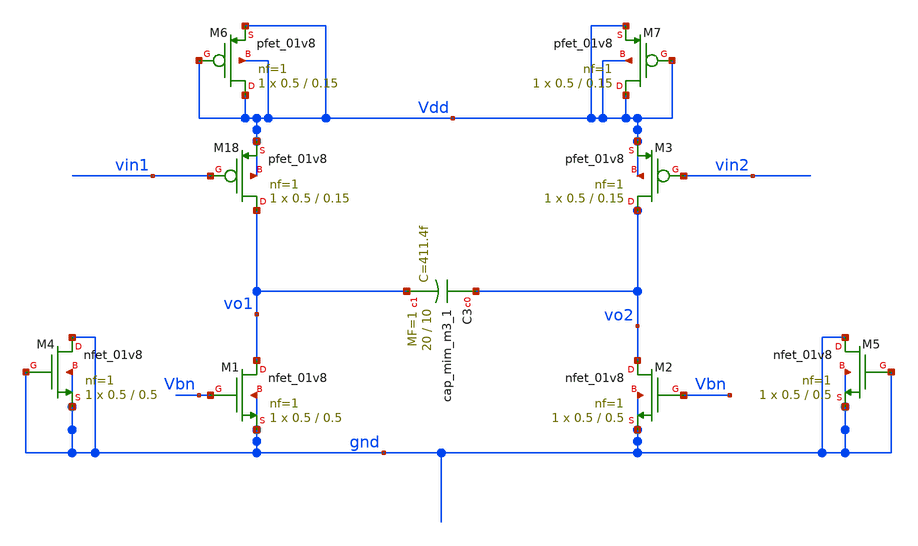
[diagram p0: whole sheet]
** sch_path: xschem/xschemfiles/integrator2.sch
**.subckt integrator2
XM3 vo2 vin2 Vdd Vdd sky130_fd_pr__pfet_01v8 L=0.15 W=0.5 nf=1 ad='int((nf+1)/2) * W/nf * 0.29' as='int((nf+2)/2) * W/nf * 0.29'
+ pd='2*int((nf+1)/2) * (W/nf + 0.29)' ps='2*int((nf+2)/2) * (W/nf + 0.29)' nrd='0.29 / W' nrs='0.29 / W'
+ sa=0 sb=0 sd=0 mult=1 m=1
XM1 vo1 Vbn gnd gnd sky130_fd_pr__nfet_01v8 L=0.5 W=0.5 nf=1 ad='int((nf+1)/2) * W/nf * 0.29' as='int((nf+2)/2) * W/nf * 0.29'
+ pd='2*int((nf+1)/2) * (W/nf + 0.29)' ps='2*int((nf+2)/2) * (W/nf + 0.29)' nrd='0.29 / W' nrs='0.29 / W'
+ sa=0 sb=0 sd=0 mult=1 m=1
XM2 vo2 Vbn gnd gnd sky130_fd_pr__nfet_01v8 L=0.5 W=0.5 nf=1 ad='int((nf+1)/2) * W/nf * 0.29' as='int((nf+2)/2) * W/nf * 0.29'
+ pd='2*int((nf+1)/2) * (W/nf + 0.29)' ps='2*int((nf+2)/2) * (W/nf + 0.29)' nrd='0.29 / W' nrs='0.29 / W'
+ sa=0 sb=0 sd=0 mult=1 m=1
XC3 vo2 vo1 sky130_fd_pr__cap_mim_m3_1 W=20 L=10 MF=1 m=1
XM18 vo1 vin1 Vdd Vdd sky130_fd_pr__pfet_01v8 L=0.15 W=0.5 nf=1 ad='int((nf+1)/2) * W/nf * 0.29' as='int((nf+2)/2) * W/nf * 0.29'
+ pd='2*int((nf+1)/2) * (W/nf + 0.29)' ps='2*int((nf+2)/2) * (W/nf + 0.29)' nrd='0.29 / W' nrs='0.29 / W'
+ sa=0 sb=0 sd=0 mult=1 m=1
XM4 gnd gnd gnd gnd sky130_fd_pr__nfet_01v8 L=0.5 W=0.5 nf=1 ad='int((nf+1)/2) * W/nf * 0.29' as='int((nf+2)/2) * W/nf * 0.29'
+ pd='2*int((nf+1)/2) * (W/nf + 0.29)' ps='2*int((nf+2)/2) * (W/nf + 0.29)' nrd='0.29 / W' nrs='0.29 / W'
+ sa=0 sb=0 sd=0 mult=1 m=1
XM5 gnd gnd gnd gnd sky130_fd_pr__nfet_01v8 L=0.5 W=0.5 nf=1 ad='int((nf+1)/2) * W/nf * 0.29' as='int((nf+2)/2) * W/nf * 0.29'
+ pd='2*int((nf+1)/2) * (W/nf + 0.29)' ps='2*int((nf+2)/2) * (W/nf + 0.29)' nrd='0.29 / W' nrs='0.29 / W'
+ sa=0 sb=0 sd=0 mult=1 m=1
XM6 Vdd Vdd Vdd Vdd sky130_fd_pr__pfet_01v8 L=0.15 W=0.5 nf=1 ad='int((nf+1)/2) * W/nf * 0.29' as='int((nf+2)/2) * W/nf * 0.29'
+ pd='2*int((nf+1)/2) * (W/nf + 0.29)' ps='2*int((nf+2)/2) * (W/nf + 0.29)' nrd='0.29 / W' nrs='0.29 / W'
+ sa=0 sb=0 sd=0 mult=1 m=1
XM7 Vdd Vdd Vdd Vdd sky130_fd_pr__pfet_01v8 L=0.15 W=0.5 nf=1 ad='int((nf+1)/2) * W/nf * 0.29' as='int((nf+2)/2) * W/nf * 0.29'
+ pd='2*int((nf+1)/2) * (W/nf + 0.29)' ps='2*int((nf+2)/2) * (W/nf + 0.29)' nrd='0.29 / W' nrs='0.29 / W'
+ sa=0 sb=0 sd=0 mult=1 m=1
**.ends
.end
